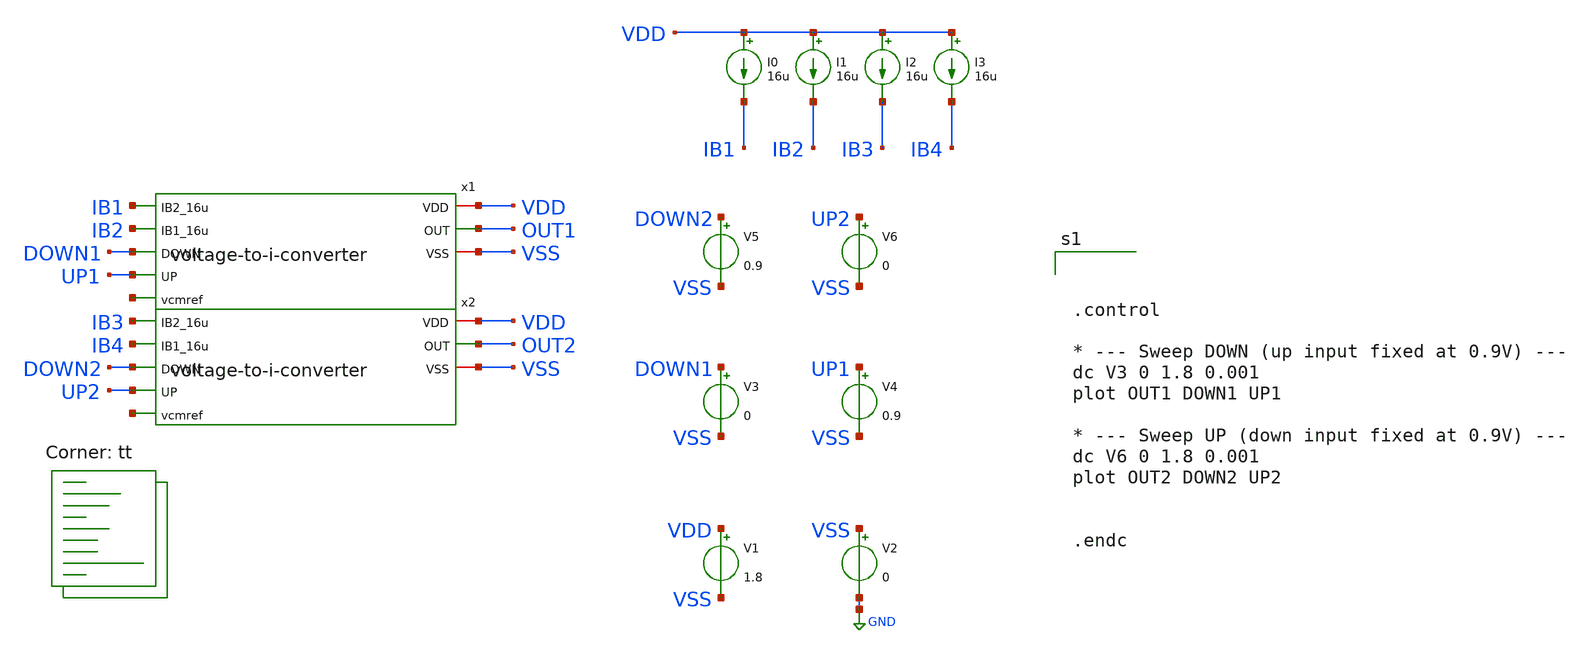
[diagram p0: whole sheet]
** sch_path: v-i-converter/tb_dc.sch
**.subckt tb_dc
V1 VDD VSS 1.8
V2 VSS GND 0
V3 DOWN1 VSS 0
V4 UP1 VSS 0.9
x1 VDD IB1 IB2 OUT1 DOWN1 UP1 net1 VSS voltage-to-i-converter
x2 VDD IB3 IB4 OUT2 DOWN2 UP2 net2 VSS voltage-to-i-converter
V5 DOWN2 VSS 0.9
V6 UP2 VSS 0
I0 VDD IB1 16u
I1 VDD IB2 16u
I2 VDD IB3 16u
I3 VDD IB4 16u
**** begin user architecture code
.lib $::SKYWATER_MODELS/sky130.lib.spice tt



.control

* --- Sweep DOWN (up input fixed at 0.9V) ---
dc V3 0 1.8 0.001
plot OUT1 DOWN1 UP1

* --- Sweep UP (down input fixed at 0.9V) ---
dc V6 0 1.8 0.001
plot OUT2 DOWN2 UP2


.endc


**** end user architecture code
**.ends

* expanding   symbol:  /foss/designs/afe-icdec-teknofest-2026/CTLE/voltage-to-i-converter.sym # of
*+ pins=8
** sym_path: CTLE/voltage-to-i-converter.sym
** sch_path: CTLE/voltage-to-i-converter.sch
.subckt voltage-to-i-converter VDD IB2_16u IB1_16u OUT DOWN UP vcmref VSS
*.iopin VDD
*.iopin VSS
*.opin OUT
*.ipin IB2_16u
*.ipin UP
*.ipin DOWN
*.ipin IB1_16u
*.ipin vcmref
XM1 net3 net3 VDD VDD sky130_fd_pr__pfet_01v8 L=0.6 W=75 nf=1 ad='int((nf+1)/2) * W/nf * 0.29' as='int((nf+2)/2) * W/nf * 0.29'
+ pd='2*int((nf+1)/2) * (W/nf + 0.29)' ps='2*int((nf+2)/2) * (W/nf + 0.29)' nrd='0.29 / W' nrs='0.29 / W'
+ sa=0 sb=0 sd=0 mult=1 m=1
XM2 net5 net5 VDD VDD sky130_fd_pr__pfet_01v8 L=0.6 W=75 nf=1 ad='int((nf+1)/2) * W/nf * 0.29' as='int((nf+2)/2) * W/nf * 0.29'
+ pd='2*int((nf+1)/2) * (W/nf + 0.29)' ps='2*int((nf+2)/2) * (W/nf + 0.29)' nrd='0.29 / W' nrs='0.29 / W'
+ sa=0 sb=0 sd=0 mult=1 m=1
XM5 net1 IB1_16u VSS VSS sky130_fd_pr__nfet_01v8 L=1.5 W=25 nf=1 ad='int((nf+1)/2) * W/nf * 0.29' as='int((nf+2)/2) * W/nf * 0.29'
+ pd='2*int((nf+1)/2) * (W/nf + 0.29)' ps='2*int((nf+2)/2) * (W/nf + 0.29)' nrd='0.29 / W' nrs='0.29 / W'
+ sa=0 sb=0 sd=0 mult=1 m=1
XM6 IB1_16u IB1_16u VSS VSS sky130_fd_pr__nfet_01v8 L=1.5 W=25 nf=1 ad='int((nf+1)/2) * W/nf * 0.29'
+ as='int((nf+2)/2) * W/nf * 0.29' pd='2*int((nf+1)/2) * (W/nf + 0.29)' ps='2*int((nf+2)/2) * (W/nf + 0.29)'
+ nrd='0.29 / W' nrs='0.29 / W' sa=0 sb=0 sd=0 mult=1 m=1
XM7 net4 net4 VDD VDD sky130_fd_pr__pfet_01v8 L=0.6 W=75 nf=1 ad='int((nf+1)/2) * W/nf * 0.29' as='int((nf+2)/2) * W/nf * 0.29'
+ pd='2*int((nf+1)/2) * (W/nf + 0.29)' ps='2*int((nf+2)/2) * (W/nf + 0.29)' nrd='0.29 / W' nrs='0.29 / W'
+ sa=0 sb=0 sd=0 mult=1 m=1
XM8 net6 net6 VDD VDD sky130_fd_pr__pfet_01v8 L=0.6 W=75 nf=1 ad='int((nf+1)/2) * W/nf * 0.29' as='int((nf+2)/2) * W/nf * 0.29'
+ pd='2*int((nf+1)/2) * (W/nf + 0.29)' ps='2*int((nf+2)/2) * (W/nf + 0.29)' nrd='0.29 / W' nrs='0.29 / W'
+ sa=0 sb=0 sd=0 mult=1 m=1
XM11 net2 IB2_16u VSS VSS sky130_fd_pr__nfet_01v8 L=1.5 W=25 nf=1 ad='int((nf+1)/2) * W/nf * 0.29' as='int((nf+2)/2) * W/nf * 0.29'
+ pd='2*int((nf+1)/2) * (W/nf + 0.29)' ps='2*int((nf+2)/2) * (W/nf + 0.29)' nrd='0.29 / W' nrs='0.29 / W'
+ sa=0 sb=0 sd=0 mult=1 m=1
XM12 IB2_16u IB2_16u VSS VSS sky130_fd_pr__nfet_01v8 L=1.5 W=25 nf=1 ad='int((nf+1)/2) * W/nf * 0.29'
+ as='int((nf+2)/2) * W/nf * 0.29' pd='2*int((nf+1)/2) * (W/nf + 0.29)' ps='2*int((nf+2)/2) * (W/nf + 0.29)'
+ nrd='0.29 / W' nrs='0.29 / W' sa=0 sb=0 sd=0 mult=1 m=1
XM13 OUT net6 VDD VDD sky130_fd_pr__pfet_01v8 L=0.6 W=75 nf=1 ad='int((nf+1)/2) * W/nf * 0.29' as='int((nf+2)/2) * W/nf * 0.29'
+ pd='2*int((nf+1)/2) * (W/nf + 0.29)' ps='2*int((nf+2)/2) * (W/nf + 0.29)' nrd='0.29 / W' nrs='0.29 / W'
+ sa=0 sb=0 sd=0 mult=1 m=1
XM14 net7 net5 VDD VDD sky130_fd_pr__pfet_01v8 L=0.6 W=75 nf=1 ad='int((nf+1)/2) * W/nf * 0.29' as='int((nf+2)/2) * W/nf * 0.29'
+ pd='2*int((nf+1)/2) * (W/nf + 0.29)' ps='2*int((nf+2)/2) * (W/nf + 0.29)' nrd='0.29 / W' nrs='0.29 / W'
+ sa=0 sb=0 sd=0 mult=1 m=1
XM15 net7 net7 VSS VSS sky130_fd_pr__nfet_01v8 L=1.5 W=25 nf=1 ad='int((nf+1)/2) * W/nf * 0.29' as='int((nf+2)/2) * W/nf * 0.29'
+ pd='2*int((nf+1)/2) * (W/nf + 0.29)' ps='2*int((nf+2)/2) * (W/nf + 0.29)' nrd='0.29 / W' nrs='0.29 / W'
+ sa=0 sb=0 sd=0 mult=1 m=1
XM16 OUT net7 VSS VSS sky130_fd_pr__nfet_01v8 L=1.5 W=25 nf=1 ad='int((nf+1)/2) * W/nf * 0.29' as='int((nf+2)/2) * W/nf * 0.29'
+ pd='2*int((nf+1)/2) * (W/nf + 0.29)' ps='2*int((nf+2)/2) * (W/nf + 0.29)' nrd='0.29 / W' nrs='0.29 / W'
+ sa=0 sb=0 sd=0 mult=1 m=1
XR1 DOWN vcmref VSS sky130_fd_pr__res_high_po_0p35 L=70 mult=1 m=1
XR2 vcmref UP VSS sky130_fd_pr__res_high_po_0p35 L=70 mult=1 m=1
XM3 net5 DOWN net1 VSS sky130_fd_pr__nfet_01v8 L=0.5 W=25 nf=1 ad='int((nf+1)/2) * W/nf * 0.29' as='int((nf+2)/2) * W/nf * 0.29'
+ pd='2*int((nf+1)/2) * (W/nf + 0.29)' ps='2*int((nf+2)/2) * (W/nf + 0.29)' nrd='0.29 / W' nrs='0.29 / W'
+ sa=0 sb=0 sd=0 mult=1 m=1
XM4 net3 vcmref net1 VSS sky130_fd_pr__nfet_01v8 L=0.5 W=25 nf=1 ad='int((nf+1)/2) * W/nf * 0.29' as='int((nf+2)/2) * W/nf * 0.29'
+ pd='2*int((nf+1)/2) * (W/nf + 0.29)' ps='2*int((nf+2)/2) * (W/nf + 0.29)' nrd='0.29 / W' nrs='0.29 / W'
+ sa=0 sb=0 sd=0 mult=1 m=1
XM9 net4 vcmref net2 VSS sky130_fd_pr__nfet_01v8 L=0.5 W=25 nf=1 ad='int((nf+1)/2) * W/nf * 0.29' as='int((nf+2)/2) * W/nf * 0.29'
+ pd='2*int((nf+1)/2) * (W/nf + 0.29)' ps='2*int((nf+2)/2) * (W/nf + 0.29)' nrd='0.29 / W' nrs='0.29 / W'
+ sa=0 sb=0 sd=0 mult=1 m=1
XM10 net6 UP net2 VSS sky130_fd_pr__nfet_01v8 L=0.5 W=25 nf=1 ad='int((nf+1)/2) * W/nf * 0.29' as='int((nf+2)/2) * W/nf * 0.29'
+ pd='2*int((nf+1)/2) * (W/nf + 0.29)' ps='2*int((nf+2)/2) * (W/nf + 0.29)' nrd='0.29 / W' nrs='0.29 / W'
+ sa=0 sb=0 sd=0 mult=1 m=1
.ends

.GLOBAL GND
.end
